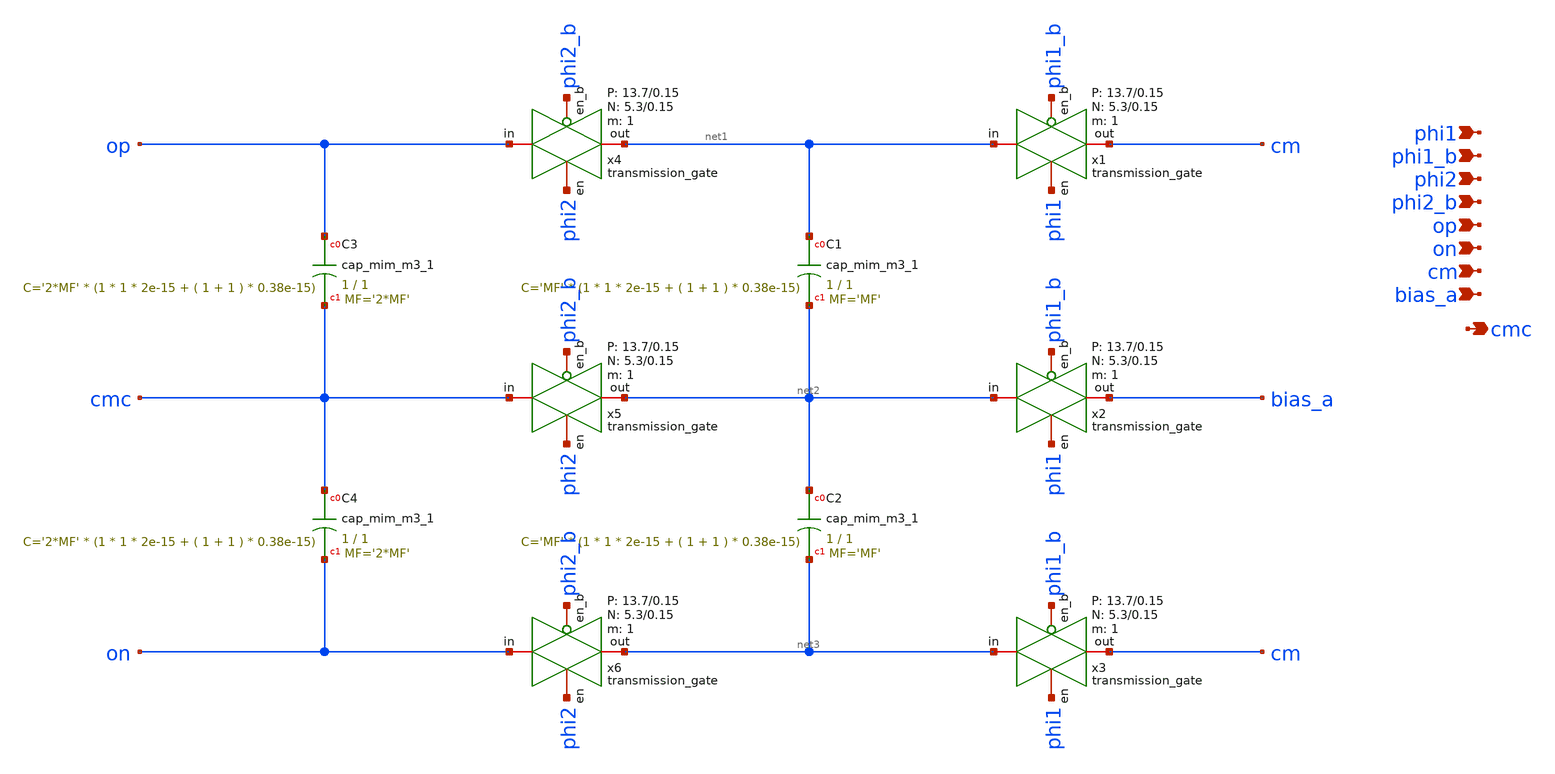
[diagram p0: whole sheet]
** sch_path: design/schematic/sc_cmfb.sch
**.subckt sc_cmfb on cm bias_a op cmc phi2_b phi2 phi1_b phi1
*.ipin on
*.ipin cm
*.ipin bias_a
*.ipin op
*.opin cmc
*.ipin phi2_b
*.ipin phi2
*.ipin phi1_b
*.ipin phi1
x1 net1 cm phi1 phi1_b VDD GND 1 5.3 0.15 13.7 0.15 transmission_gate
x2 net2 bias_a phi1 phi1_b VDD GND 1 5.3 0.15 13.7 0.15 transmission_gate
x3 net3 cm phi1 phi1_b VDD GND 1 5.3 0.15 13.7 0.15 transmission_gate
x4 op net1 phi2 phi2_b VDD GND 1 5.3 0.15 13.7 0.15 transmission_gate
x5 cmc net2 phi2 phi2_b VDD GND 1 5.3 0.15 13.7 0.15 transmission_gate
x6 on net3 phi2 phi2_b VDD GND 1 5.3 0.15 13.7 0.15 transmission_gate
XC1 net1 net2 sky130_fd_pr__cap_mim_m3_1 W=1 L=1 MF='MF' m='MF'
XC2 net2 net3 sky130_fd_pr__cap_mim_m3_1 W=1 L=1 MF='MF' m='MF'
XC3 op cmc sky130_fd_pr__cap_mim_m3_1 W=1 L=1 MF='2*MF' m='2*MF'
XC4 cmc on sky130_fd_pr__cap_mim_m3_1 W=1 L=1 MF='2*MF' m='2*MF'
**.ends

* expanding   symbol:  transmission_gate.sym # of pins=4
** sym_path: design/schematic/transmission_gate.sym
** sch_path: design/schematic/transmission_gate.sch
.subckt transmission_gate in out en en_b VDD VSS N W_N L_N W_P L_P    N=1 W_N=5.3 L_N=0.15 W_P=13.7
+ L_P=0.15
*.iopin in
*.iopin out
*.ipin en
*.ipin en_b
XM1 out en in VSS sky130_fd_pr__nfet_01v8 L=L_N W=W_N nf=1 ad='int((nf+1)/2) * W/nf * 0.29' as='int((nf+2)/2) * W/nf * 0.29'
+ pd='2*int((nf+1)/2) * (W/nf + 0.29)' ps='2*int((nf+2)/2) * (W/nf + 0.29)' nrd='0.29 / W' nrs='0.29 / W'
+ sa=0 sb=0 sd=0 mult=N m=N
XM2 out en_b in VDD sky130_fd_pr__pfet_01v8 L=L_P W=W_P nf=1 ad='int((nf+1)/2) * W/nf * 0.29' as='int((nf+2)/2) * W/nf * 0.29'
+ pd='2*int((nf+1)/2) * (W/nf + 0.29)' ps='2*int((nf+2)/2) * (W/nf + 0.29)' nrd='0.29 / W' nrs='0.29 / W'
+ sa=0 sb=0 sd=0 mult=N m=N
.ends

.end
